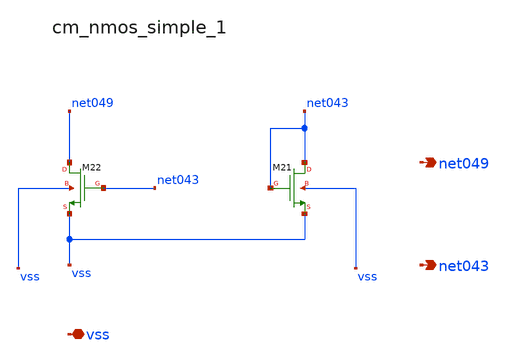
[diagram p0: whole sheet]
** sch_path: analog-db/raw/amp_015_sau_cfcc/hier/blocks/cm_nmos_simple_1.sch
**.subckt cm_nmos_simple_1 vss net049 net043
*.iopin vss
*.opin net049
*.opin net043
XM21 net043 net043 vss vss sg13_lv_nmos w=x_dut_xm21_w l=x_dut_xm21_l ng=1 m=x_dut_xm21_m
XM22 net049 net043 vss vss sg13_lv_nmos w=x_dut_xm22_w l=x_dut_xm22_l ng=1 m=x_dut_xm22_m
**.ends
.end
